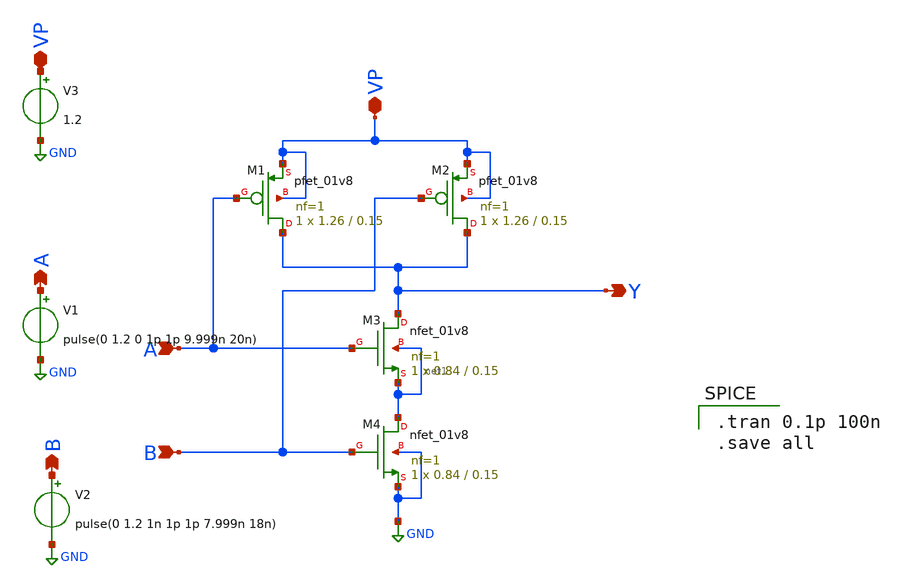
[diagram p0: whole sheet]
** sch_path: component/NAND2/NAND_sch_test.sch
**.subckt NAND_sch_test VP A B Y VP B Y A
*.iopin VP
*.ipin A
*.ipin B
*.opin Y
*.iopin VP
*.opin B
*.opin Y
*.opin A
XM1 Y A VP VP sky130_fd_pr__pfet_01v8 L=0.15 W=1.26 nf=1 ad='int((nf+1)/2) * W/nf * 0.29' as='int((nf+2)/2) * W/nf * 0.29'
+ pd='2*int((nf+1)/2) * (W/nf + 0.29)' ps='2*int((nf+2)/2) * (W/nf + 0.29)' nrd='0.29 / W' nrs='0.29 / W'
+ sa=0 sb=0 sd=0 mult=1 m=1
XM2 Y B VP VP sky130_fd_pr__pfet_01v8 L=0.15 W=1.26 nf=1 ad='int((nf+1)/2) * W/nf * 0.29' as='int((nf+2)/2) * W/nf * 0.29'
+ pd='2*int((nf+1)/2) * (W/nf + 0.29)' ps='2*int((nf+2)/2) * (W/nf + 0.29)' nrd='0.29 / W' nrs='0.29 / W'
+ sa=0 sb=0 sd=0 mult=1 m=1
XM3 Y A net1 net1 sky130_fd_pr__nfet_01v8 L=0.15 W=0.84 nf=1 ad='int((nf+1)/2) * W/nf * 0.29' as='int((nf+2)/2) * W/nf * 0.29'
+ pd='2*int((nf+1)/2) * (W/nf + 0.29)' ps='2*int((nf+2)/2) * (W/nf + 0.29)' nrd='0.29 / W' nrs='0.29 / W'
+ sa=0 sb=0 sd=0 mult=1 m=1
XM4 net1 B GND GND sky130_fd_pr__nfet_01v8 L=0.15 W=0.84 nf=1 ad='int((nf+1)/2) * W/nf * 0.29' as='int((nf+2)/2) * W/nf * 0.29'
+ pd='2*int((nf+1)/2) * (W/nf + 0.29)' ps='2*int((nf+2)/2) * (W/nf + 0.29)' nrd='0.29 / W' nrs='0.29 / W'
+ sa=0 sb=0 sd=0 mult=1 m=1
V1 A GND pulse(0 1.2 0 1p 1p 9.999n 20n)
V2 B GND pulse(0 1.2 1n 1p 1p 7.999n 18n)
V3 VP GND 1.2
**** begin user architecture code

** opencircuitdesign pdks install
.lib $::SKYWATER_MODELS/sky130.lib.spice tt



.tran 0.1p 100n
.save all

**** end user architecture code
**.ends
.GLOBAL GND
.end
